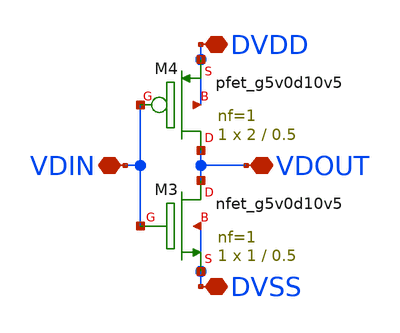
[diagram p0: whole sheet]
** sch_path: xschem/5V_Inverter1.sch
**.subckt 5V_Inverter1 VDOUT VDIN DVDD DVSS
*.iopin VDOUT
*.iopin VDIN
*.iopin DVDD
*.iopin DVSS
XM3 VDOUT VDIN DVSS DVSS sky130_fd_pr__nfet_g5v0d10v5 L=0.5 W=1 nf=1 ad='int((nf+1)/2) * W/nf * 0.29'
+ as='int((nf+2)/2) * W/nf * 0.29' pd='2*int((nf+1)/2) * (W/nf + 0.29)' ps='2*int((nf+2)/2) * (W/nf + 0.29)'
+ nrd='0.29 / W' nrs='0.29 / W' sa=0 sb=0 sd=0 mult=1 m=1
XM4 VDOUT VDIN DVDD DVDD sky130_fd_pr__pfet_g5v0d10v5 L=0.5 W=2 nf=1 ad='int((nf+1)/2) * W/nf * 0.29'
+ as='int((nf+2)/2) * W/nf * 0.29' pd='2*int((nf+1)/2) * (W/nf + 0.29)' ps='2*int((nf+2)/2) * (W/nf + 0.29)'
+ nrd='0.29 / W' nrs='0.29 / W' sa=0 sb=0 sd=0 mult=1 m=1
**.ends
.end
